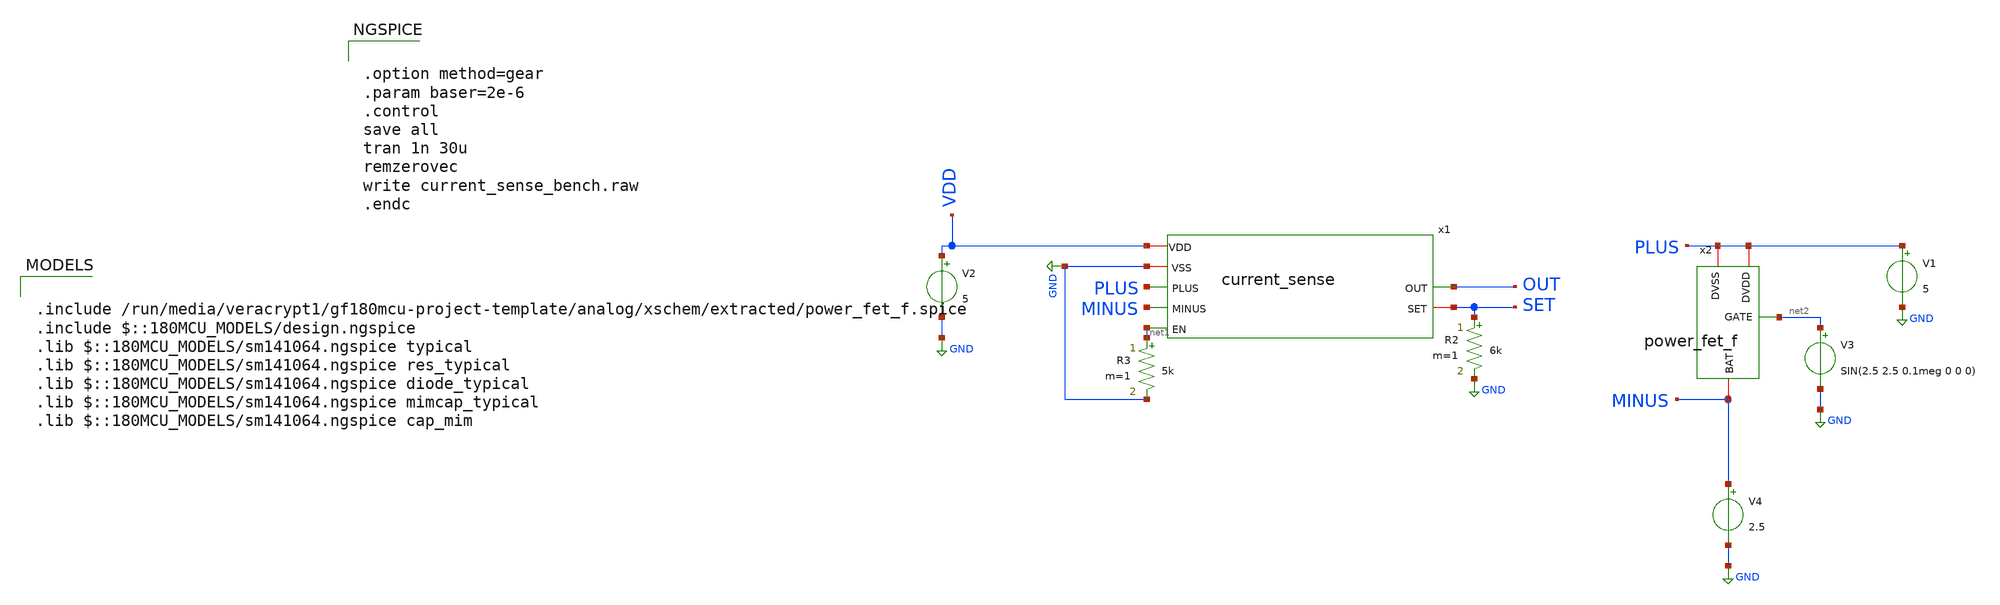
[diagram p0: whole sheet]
** sch_path: analog/xschem/old/current_sense_bench.sch
**.subckt current_sense_bench
V2 VDD GND 5
x1 VDD GND PLUS OUT SET MINUS net1 current_sense
V1 PLUS GND 5
V3 net2 GND SIN(2.5 2.5 0.1meg 0 0 0)
R2 SET GND 6k m=1
R3 net1 GND 5k m=1
V4 MINUS GND 2.5
x2 PLUS PLUS MINUS net2 power_fet_f
**** begin user architecture code


.option method=gear
.param baser=2e-6
.control
save all
tran 1n 30u
remzerovec
write current_sense_bench.raw
.endc



.include /run/media/veracrypt1/gf180mcu-project-template/analog/xschem/extracted/power_fet_f.spice
.include $::180MCU_MODELS/design.ngspice
.lib $::180MCU_MODELS/sm141064.ngspice typical
.lib $::180MCU_MODELS/sm141064.ngspice res_typical
.lib $::180MCU_MODELS/sm141064.ngspice diode_typical
.lib $::180MCU_MODELS/sm141064.ngspice mimcap_typical
.lib $::180MCU_MODELS/sm141064.ngspice cap_mim

**** end user architecture code
**.ends
.GLOBAL GND
.end
